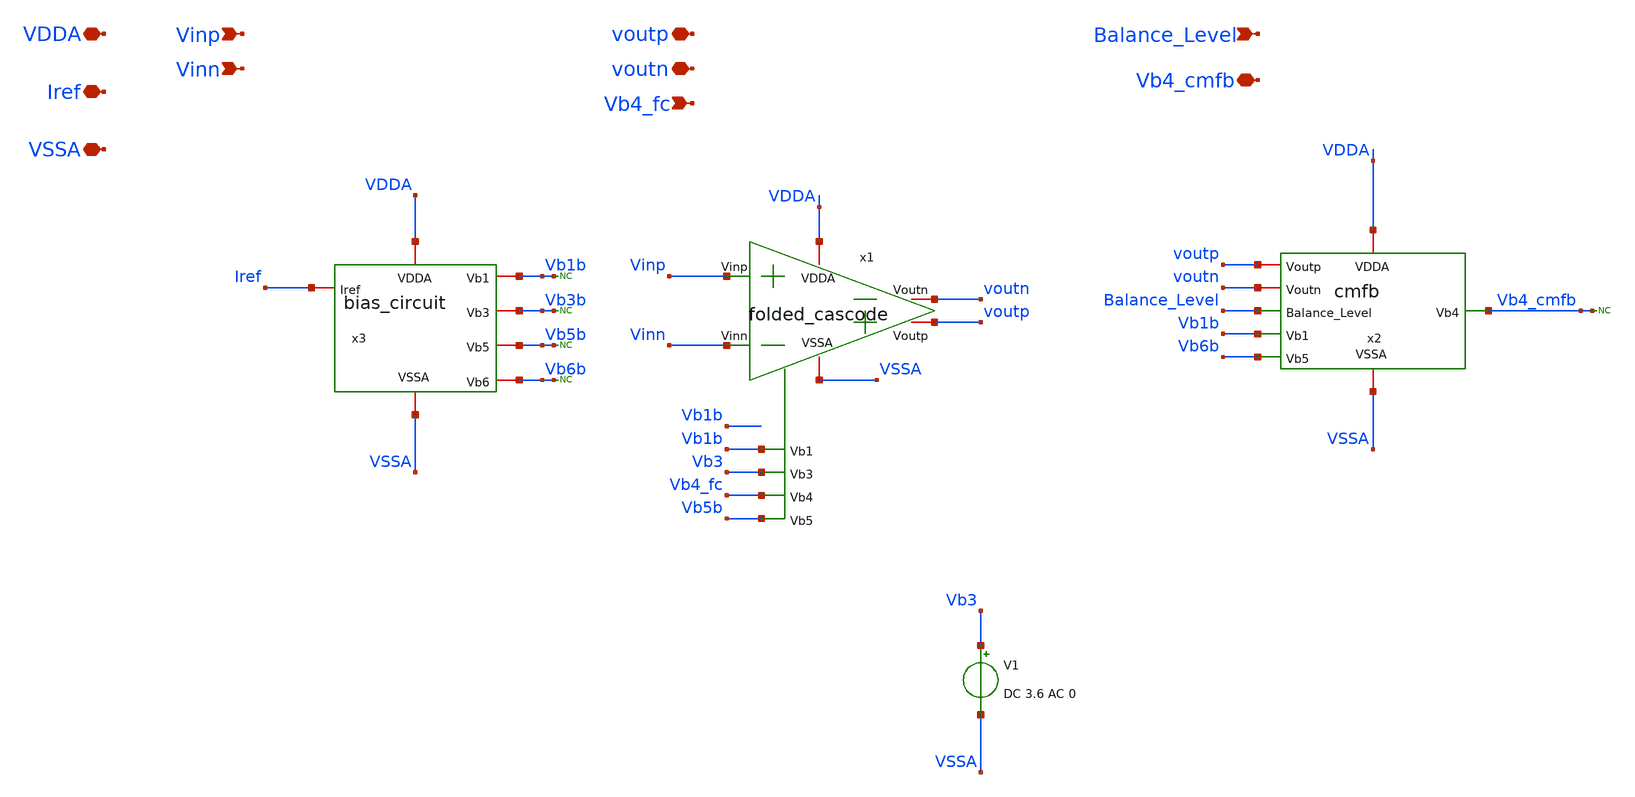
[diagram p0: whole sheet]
** sch_path: Folded_cascode/schematic/top_fc_stb.sch
**.subckt top_fc_stb Iref VDDA VSSA Vinp Vinn Balance_Level voutp voutn Vb4_fc Vb4_cmfb
*.iopin Iref
*.iopin VDDA
*.iopin VSSA
*.ipin Vinp
*.ipin Vinn
*.ipin Balance_Level
*.iopin voutp
*.iopin voutn
*.ipin Vb4_fc
*.iopin Vb4_cmfb
x1 VDDA VSSA Vinp Vinn voutp voutn Vb1b Vb3 Vb4_fc Vb5b folded_cascode
x2 VDDA VSSA voutp voutn Balance_Level Vb1b Vb4_cmfb Vb6b cmfb
* noconn Vb3b
V1 Vb3 VSSA DC 3.6 AC 0
* noconn Vb5b
* noconn Vb1b
* noconn Vb6b
x3 VDDA Vb3b Vb1b Vb5b VSSA Iref Vb6b bias_circuit
* noconn Vb4_cmfb
**.ends
.end
